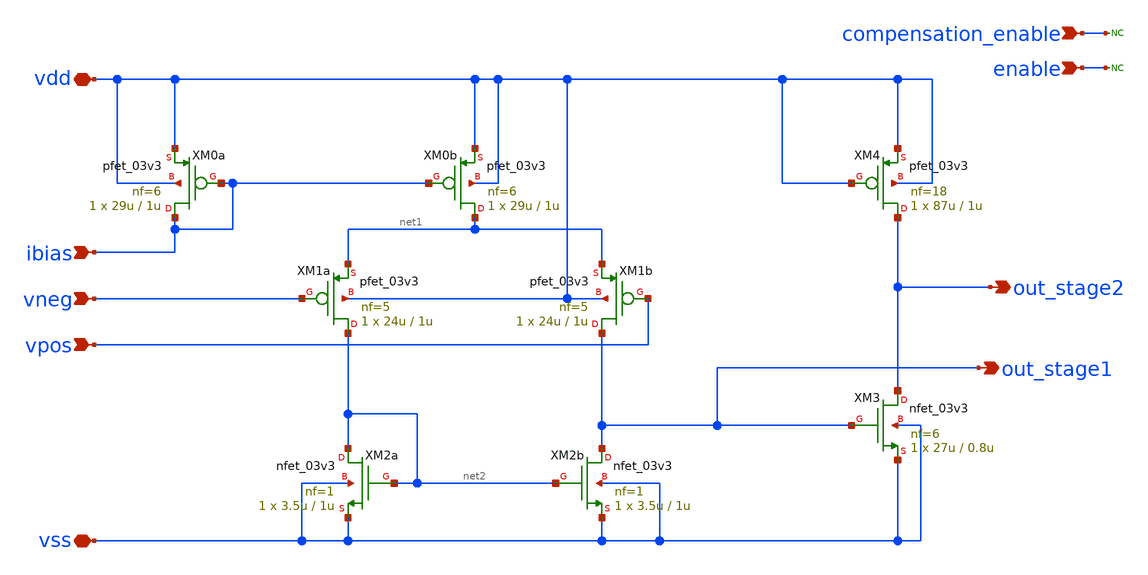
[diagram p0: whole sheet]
** sch_path: DESIGN/DACFUTURE_EDU/Two_stage_OTA/two_stage_ota.sch
**.subckt two_stage_ota enable vpos vneg vdd vss compensation_enable out_stage2 ibias
*.ipin enable
*.ipin vpos
*.ipin vneg
*.iopin vdd
*.iopin vss
*.ipin compensation_enable
*.opin out_stage2
*.ipin ibias
* noconn compensation_enable
* noconn enable
XM0b net1 ibias vdd vdd pfet_03v3 L=1u W=29u nf=6 ad='int((nf+1)/2) * W/nf * 0.18u' as='int((nf+2)/2) * W/nf * 0.18u'
+ pd='2*int((nf+1)/2) * (W/nf + 0.18u)' ps='2*int((nf+2)/2) * (W/nf + 0.18u)' nrd='0.18u / W' nrs='0.18u / W'
+ sa=0 sb=0 sd=0 m=1
XM0a ibias ibias vdd vdd pfet_03v3 L=1u W=29u nf=6 ad='int((nf+1)/2) * W/nf * 0.18u' as='int((nf+2)/2) * W/nf * 0.18u'
+ pd='2*int((nf+1)/2) * (W/nf + 0.18u)' ps='2*int((nf+2)/2) * (W/nf + 0.18u)' nrd='0.18u / W' nrs='0.18u / W'
+ sa=0 sb=0 sd=0 m=1
XM4 out_stage2 vdd vdd vdd pfet_03v3 L=1u W=87u nf=18 ad='int((nf+1)/2) * W/nf * 0.18u' as='int((nf+2)/2) * W/nf * 0.18u'
+ pd='2*int((nf+1)/2) * (W/nf + 0.18u)' ps='2*int((nf+2)/2) * (W/nf + 0.18u)' nrd='0.18u / W' nrs='0.18u / W'
+ sa=0 sb=0 sd=0 m=1
XM1a net2 vneg net1 vdd pfet_03v3 L=1u W=24u nf=5 ad='int((nf+1)/2) * W/nf * 0.18u' as='int((nf+2)/2) * W/nf * 0.18u'
+ pd='2*int((nf+1)/2) * (W/nf + 0.18u)' ps='2*int((nf+2)/2) * (W/nf + 0.18u)' nrd='0.18u / W' nrs='0.18u / W'
+ sa=0 sb=0 sd=0 m=1
XM1b out_stage1 vpos net1 vdd pfet_03v3 L=1u W=24u nf=5 ad='int((nf+1)/2) * W/nf * 0.18u' as='int((nf+2)/2) * W/nf * 0.18u'
+ pd='2*int((nf+1)/2) * (W/nf + 0.18u)' ps='2*int((nf+2)/2) * (W/nf + 0.18u)' nrd='0.18u / W' nrs='0.18u / W'
+ sa=0 sb=0 sd=0 m=1
XM2b out_stage1 net2 vss vss nfet_03v3 L=1u W=3.5u nf=1 ad='int((nf+1)/2) * W/nf * 0.18u' as='int((nf+2)/2) * W/nf * 0.18u'
+ pd='2*int((nf+1)/2) * (W/nf + 0.18u)' ps='2*int((nf+2)/2) * (W/nf + 0.18u)' nrd='0.18u / W' nrs='0.18u / W'
+ sa=0 sb=0 sd=0 m=1
XM3 out_stage2 out_stage1 vss vss nfet_03v3 L=0.8u W=27u nf=6 ad='int((nf+1)/2) * W/nf * 0.18u' as='int((nf+2)/2) * W/nf * 0.18u'
+ pd='2*int((nf+1)/2) * (W/nf + 0.18u)' ps='2*int((nf+2)/2) * (W/nf + 0.18u)' nrd='0.18u / W' nrs='0.18u / W'
+ sa=0 sb=0 sd=0 m=1
XM2a net2 net2 vss vss nfet_03v3 L=1u W=3.5u nf=1 ad='int((nf+1)/2) * W/nf * 0.18u' as='int((nf+2)/2) * W/nf * 0.18u'
+ pd='2*int((nf+1)/2) * (W/nf + 0.18u)' ps='2*int((nf+2)/2) * (W/nf + 0.18u)' nrd='0.18u / W' nrs='0.18u / W'
+ sa=0 sb=0 sd=0 m=1
**.ends
.end
